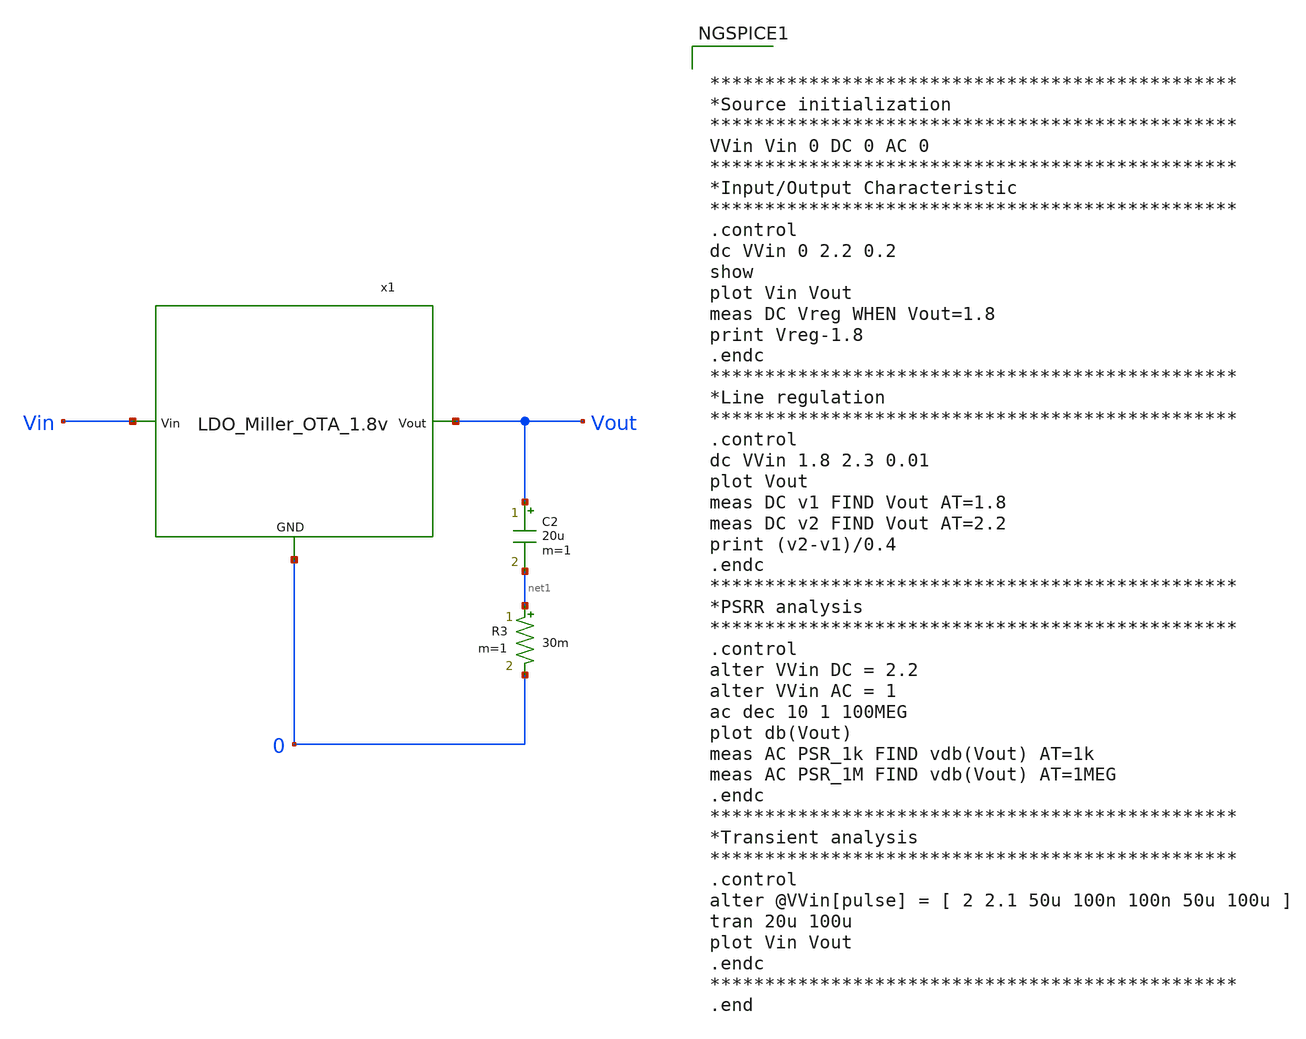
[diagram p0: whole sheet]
** sch_path: Analog_Blocks/LDO/Testbench/LDO_Miller_1.8v_meas.sch
**.subckt LDO_Miller_1.8v_meas
C2 Vout net1 20u m=1
R3 net1 0 30m m=1
x1 Vin Vout 0 LDO_Miller_OTA_1.8v
**** begin user architecture code

.include $::SKYWATER_MODELS/cells/nfet_01v8/sky130_fd_pr__nfet_01v8__tt.corner.spice
.include $::SKYWATER_MODELS/cells/nfet_01v8_lvt/sky130_fd_pr__nfet_01v8_lvt__tt.corner.spice
.include $::SKYWATER_MODELS/cells/pfet_01v8/sky130_fd_pr__pfet_01v8__tt.corner.spice
.include $::SKYWATER_MODELS/cells/nfet_03v3_nvt/sky130_fd_pr__nfet_03v3_nvt__tt.corner.spice
.include $::SKYWATER_MODELS/cells/nfet_05v0_nvt/sky130_fd_pr__nfet_05v0_nvt__tt.corner.spice
.include $::SKYWATER_MODELS/cells/esd_nfet_01v8/sky130_fd_pr__esd_nfet_01v8__tt.corner.spice
.include $::SKYWATER_MODELS/cells/pfet_01v8_lvt/sky130_fd_pr__pfet_01v8_lvt__tt.corner.spice
.include $::SKYWATER_MODELS/cells/pfet_01v8_hvt/sky130_fd_pr__pfet_01v8_hvt__tt.corner.spice
.include $::SKYWATER_MODELS/cells/esd_pfet_g5v0d10v5/sky130_fd_pr__esd_pfet_g5v0d10v5__tt.corner.spice
.include $::SKYWATER_MODELS/cells/pfet_g5v0d10v5/sky130_fd_pr__pfet_g5v0d10v5__tt.corner.spice
.include $::SKYWATER_MODELS/cells/pfet_g5v0d16v0/sky130_fd_pr__pfet_g5v0d16v0__tt.corner.spice
.include $::SKYWATER_MODELS/cells/nfet_g5v0d10v5/sky130_fd_pr__nfet_g5v0d10v5__tt.corner.spice
.include $::SKYWATER_MODELS/cells/nfet_g5v0d16v0/sky130_fd_pr__nfet_g5v0d16v0__tt_discrete.corner.spice
.include $::SKYWATER_MODELS/cells/esd_nfet_g5v0d10v5/sky130_fd_pr__esd_nfet_g5v0d10v5__tt.corner.spice
.include $::SKYWATER_MODELS/models/corners/tt/nonfet.spice
* Mismatch parameters
.include $::SKYWATER_MODELS/cells/nfet_01v8/sky130_fd_pr__nfet_01v8__mismatch.corner.spice
.include $::SKYWATER_MODELS/cells/pfet_01v8/sky130_fd_pr__pfet_01v8__mismatch.corner.spice
.include $::SKYWATER_MODELS/cells/nfet_01v8_lvt/sky130_fd_pr__nfet_01v8_lvt__mismatch.corner.spice
.include $::SKYWATER_MODELS/cells/pfet_01v8_lvt/sky130_fd_pr__pfet_01v8_lvt__mismatch.corner.spice
.include $::SKYWATER_MODELS/cells/pfet_01v8_hvt/sky130_fd_pr__pfet_01v8_hvt__mismatch.corner.spice
.include $::SKYWATER_MODELS/cells/nfet_g5v0d10v5/sky130_fd_pr__nfet_g5v0d10v5__mismatch.corner.spice
.include $::SKYWATER_MODELS/cells/pfet_g5v0d10v5/sky130_fd_pr__pfet_g5v0d10v5__mismatch.corner.spice
.include $::SKYWATER_MODELS/cells/nfet_05v0_nvt/sky130_fd_pr__nfet_05v0_nvt__mismatch.corner.spice
.include $::SKYWATER_MODELS/cells/nfet_03v3_nvt/sky130_fd_pr__nfet_03v3_nvt__mismatch.corner.spice
* Resistor$::SKYWATER_MODELS/Capacitor
.include $::SKYWATER_MODELS/models/r+c/res_typical__cap_typical.spice
.include $::SKYWATER_MODELS/models/r+c/res_typical__cap_typical__lin.spice
* Special cells
.include $::SKYWATER_MODELS/models/corners/tt/specialized_cells.spice
* All models
.include $::SKYWATER_MODELS/models/all.spice
* Corner
.include $::SKYWATER_MODELS/models/corners/tt/rf.spice



************************************************
*Source initialization
************************************************
VVin Vin 0 DC 0 AC 0
************************************************
*Input/Output Characteristic
************************************************
.control
dc VVin 0 2.2 0.2
show
plot Vin Vout
meas DC Vreg WHEN Vout=1.8
print Vreg-1.8
.endc
************************************************
*Line regulation
************************************************
.control
dc VVin 1.8 2.3 0.01
plot Vout
meas DC v1 FIND Vout AT=1.8
meas DC v2 FIND Vout AT=2.2
print (v2-v1)/0.4
.endc
************************************************
*PSRR analysis
************************************************
.control
alter VVin DC = 2.2
alter VVin AC = 1
ac dec 10 1 100MEG
plot db(Vout)
meas AC PSR_1k FIND vdb(Vout) AT=1k
meas AC PSR_1M FIND vdb(Vout) AT=1MEG
.endc
************************************************
*Transient analysis
************************************************
.control
alter @VVin[pulse] = [ 2 2.1 50u 100n 100n 50u 100u ]
tran 20u 100u
plot Vin Vout
.endc
************************************************
.end


**** end user architecture code
**.ends
.end
